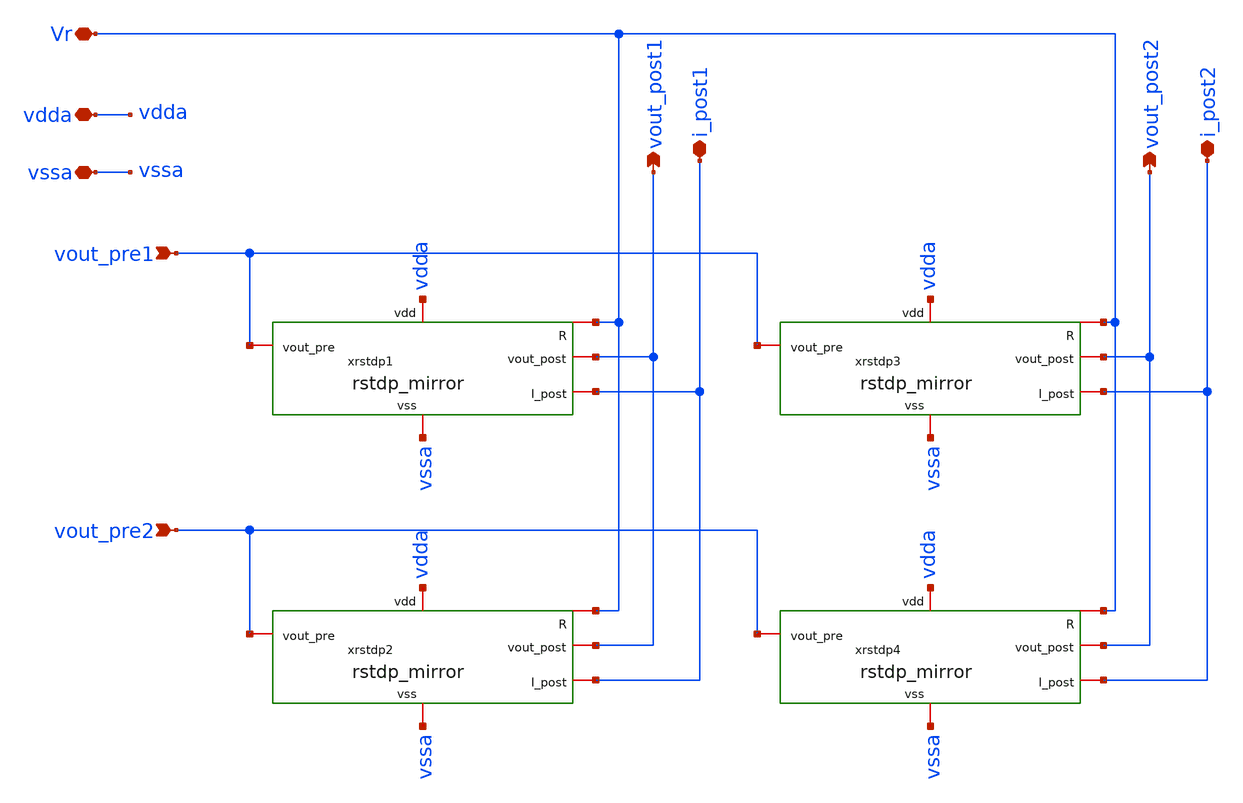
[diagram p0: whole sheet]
** sch_path: Synapse/rstdp_array_2x2.sch
**.subckt rstdp_array_2x2 vout_pre1 vout_post1 vdda vssa i_post1 vout_pre2 vout_post2 i_post2 Vr
*.ipin vout_pre1
*.opin vout_post1
*.iopin vdda
*.iopin vssa
*.iopin i_post1
*.ipin vout_pre2
*.opin vout_post2
*.iopin i_post2
*.iopin Vr
xrstdp1 vdda Vr vssa vout_pre1 vout_post1 i_post1 rstdp_mirror
xrstdp2 vdda Vr vssa vout_pre2 vout_post1 i_post1 rstdp_mirror
xrstdp3 vdda Vr vssa vout_pre1 vout_post2 i_post2 rstdp_mirror
xrstdp4 vdda Vr vssa vout_pre2 vout_post2 i_post2 rstdp_mirror
**.ends

* expanding   symbol:  rstdp_mirror.sym # of pins=6
** sym_path: Synapse/rstdp_mirror.sym
** sch_path: Synapse/rstdp_mirror.sch
.subckt rstdp_mirror vdd R vss vout_pre vout_post I_post
*.iopin vdd
*.iopin vss
*.iopin R
*.iopin vout_post
*.iopin vout_pre
*.iopin I_post
XM2 A vout_pre vpre vss sky130_fd_pr__nfet_01v8 L=0.15 W=7.5 nf=1 ad='int((nf+1)/2) * W/nf * 0.29' as='int((nf+2)/2) * W/nf * 0.29'
+ pd='2*int((nf+1)/2) * (W/nf + 0.29)' ps='2*int((nf+2)/2) * (W/nf + 0.29)' nrd='0.29 / W' nrs='0.29 / W'
+ sa=0 sb=0 sd=0 mult=1 m=1
XM3 vpre vout_post vss vss sky130_fd_pr__nfet_01v8 L=0.15 W=7.5 nf=1 ad='int((nf+1)/2) * W/nf * 0.29'
+ as='int((nf+2)/2) * W/nf * 0.29' pd='2*int((nf+1)/2) * (W/nf + 0.29)' ps='2*int((nf+2)/2) * (W/nf + 0.29)'
+ nrd='0.29 / W' nrs='0.29 / W' sa=0 sb=0 sd=0 mult=1 m=1
XM1 A vout_post vpost vss sky130_fd_pr__nfet_01v8 L=0.15 W=7.5 nf=1 ad='int((nf+1)/2) * W/nf * 0.29'
+ as='int((nf+2)/2) * W/nf * 0.29' pd='2*int((nf+1)/2) * (W/nf + 0.29)' ps='2*int((nf+2)/2) * (W/nf + 0.29)'
+ nrd='0.29 / W' nrs='0.29 / W' sa=0 sb=0 sd=0 mult=1 m=1
XM4 vpost vout_pre vss vss sky130_fd_pr__nfet_01v8 L=0.15 W=7.5 nf=1 ad='int((nf+1)/2) * W/nf * 0.29'
+ as='int((nf+2)/2) * W/nf * 0.29' pd='2*int((nf+1)/2) * (W/nf + 0.29)' ps='2*int((nf+2)/2) * (W/nf + 0.29)'
+ nrd='0.29 / W' nrs='0.29 / W' sa=0 sb=0 sd=0 mult=1 m=1
XR2 te be rram_v0
XM5 vpre R be vss sky130_fd_pr__nfet_01v8 L=0.15 W=7.5 nf=1 ad='int((nf+1)/2) * W/nf * 0.29' as='int((nf+2)/2) * W/nf * 0.29'
+ pd='2*int((nf+1)/2) * (W/nf + 0.29)' ps='2*int((nf+2)/2) * (W/nf + 0.29)' nrd='0.29 / W' nrs='0.29 / W'
+ sa=0 sb=0 sd=0 mult=1 m=1
XM6 te R vpost vss sky130_fd_pr__nfet_01v8 L=0.15 W=7.5 nf=1 ad='int((nf+1)/2) * W/nf * 0.29' as='int((nf+2)/2) * W/nf * 0.29'
+ pd='2*int((nf+1)/2) * (W/nf + 0.29)' ps='2*int((nf+2)/2) * (W/nf + 0.29)' nrd='0.29 / W' nrs='0.29 / W'
+ sa=0 sb=0 sd=0 mult=1 m=1
XM7 vpre R te vdd sky130_fd_pr__pfet_01v8 L=0.15 W=15 nf=1 ad='int((nf+1)/2) * W/nf * 0.29' as='int((nf+2)/2) * W/nf * 0.29'
+ pd='2*int((nf+1)/2) * (W/nf + 0.29)' ps='2*int((nf+2)/2) * (W/nf + 0.29)' nrd='0.29 / W' nrs='0.29 / W'
+ sa=0 sb=0 sd=0 mult=1 m=1
XM8 be R vpost vdd sky130_fd_pr__pfet_01v8 L=0.15 W=15 nf=1 ad='int((nf+1)/2) * W/nf * 0.29' as='int((nf+2)/2) * W/nf * 0.29'
+ pd='2*int((nf+1)/2) * (W/nf + 0.29)' ps='2*int((nf+2)/2) * (W/nf + 0.29)' nrd='0.29 / W' nrs='0.29 / W'
+ sa=0 sb=0 sd=0 mult=1 m=1
XM14 I_post A vdd vdd sky130_fd_pr__pfet_01v8 L=4.5 W=0.5 nf=1 ad='int((nf+1)/2) * W/nf * 0.29' as='int((nf+2)/2) * W/nf * 0.29'
+ pd='2*int((nf+1)/2) * (W/nf + 0.29)' ps='2*int((nf+2)/2) * (W/nf + 0.29)' nrd='0.29 / W' nrs='0.29 / W'
+ sa=0 sb=0 sd=0 mult=1 m=1
XM15 A A vdd vdd sky130_fd_pr__pfet_01v8 L=0.15 W=2.5 nf=1 ad='int((nf+1)/2) * W/nf * 0.29' as='int((nf+2)/2) * W/nf * 0.29'
+ pd='2*int((nf+1)/2) * (W/nf + 0.29)' ps='2*int((nf+2)/2) * (W/nf + 0.29)' nrd='0.29 / W' nrs='0.29 / W'
+ sa=0 sb=0 sd=0 mult=1 m=1
.ends

.end
